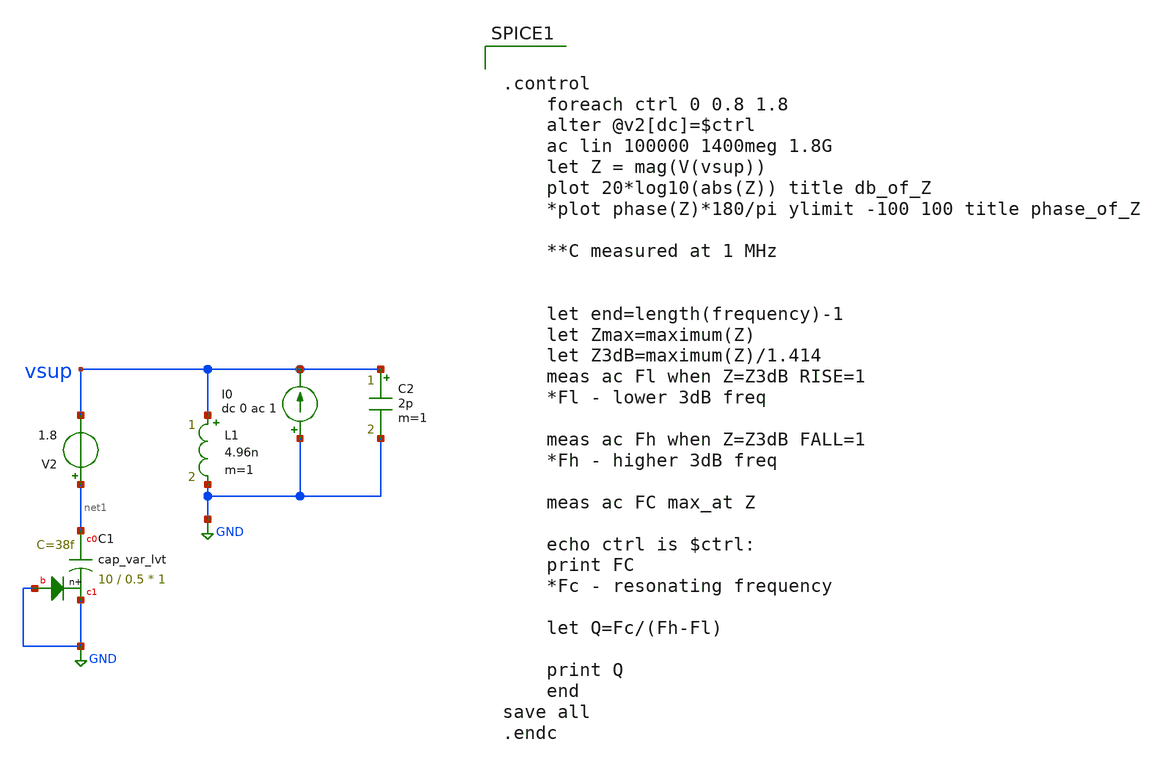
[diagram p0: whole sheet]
** sch_path: varactor_meas/vartankfin.sch
**.subckt vartankfin
I0 GND vsup dc 0 ac 1
XC1 net1 GND GND sky130_fd_pr__cap_var_lvt W=10 L=0.5 VM=1 m=1
V2 net1 vsup 1.8
C2 vsup GND 2p m=1
L1 vsup GND 4.96n m=1
**** begin user architecture code


.option wnflag = 1
.lib /usr/local/share/pdk/sky130A/libs.tech/ngspice/sky130.lib.spice tt
.include /usr/local/share/pdk/sky130A/libs.ref/sky130_fd_pr/spice/sky130_fd_pr__ind_05_220.model.spice
.param mc_mm_switch=0




.control
	foreach ctrl 0 0.8 1.8
	alter @v2[dc]=$ctrl
	ac lin 100000 1400meg 1.8G
	let Z = mag(V(vsup))
	plot 20*log10(abs(Z)) title db_of_Z
	*plot phase(Z)*180/pi ylimit -100 100 title phase_of_Z

	**C measured at 1 MHz


	let end=length(frequency)-1
	let Zmax=maximum(Z)
	let Z3dB=maximum(Z)/1.414
	meas ac Fl when Z=Z3dB RISE=1
	*Fl - lower 3dB freq

	meas ac Fh when Z=Z3dB FALL=1
	*Fh - higher 3dB freq

	meas ac FC max_at Z

	echo ctrl is $ctrl:
	print FC
	*Fc - resonating frequency

	let Q=Fc/(Fh-Fl)

	print Q
	end
save all
.endc


**** end user architecture code
**.ends
.GLOBAL GND
.end
